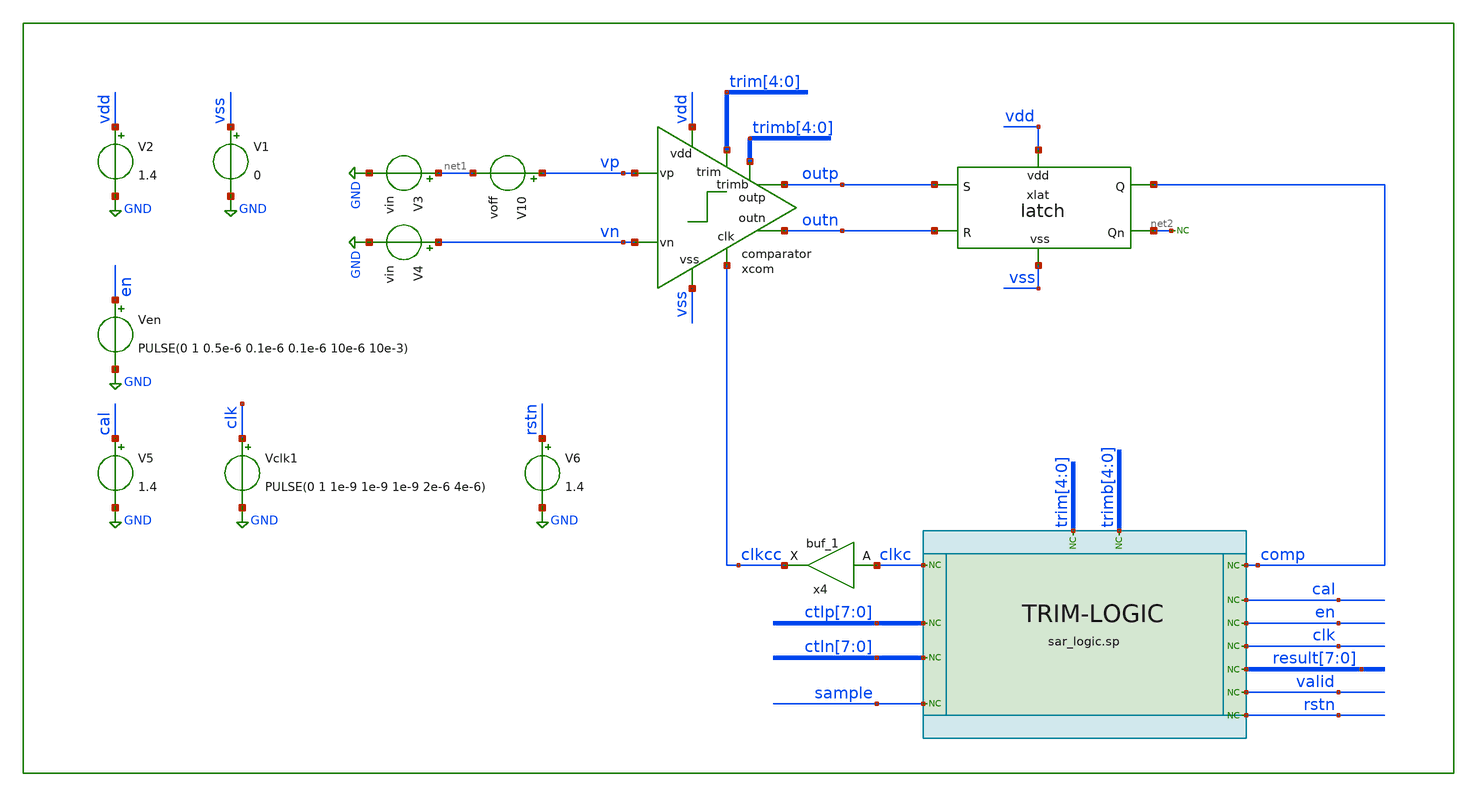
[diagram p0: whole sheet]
** sch_path: xschem/tb/comparator/tran_comparator_trim.sch
**.subckt tran_comparator_trim
xcom vss vdd clkcc outp vp outn vn trim[4] trim[3] trim[2] trim[1] trim[0] trimb[4] trimb[3]
+ trimb[2] trimb[1] trimb[0] comparator
V1 vss GND 0
V2 vdd GND 1.4
V3 net1 GND vin
V4 vn GND vin
V10 vp net1 voff
* noconn comp
x4 clkc vss vss vdd vdd clkcc sky130_fd_sc_hd__buf_1
* noconn sample
* noconn ctln[7:0]
* noconn ctlp[7:0]
* noconn trim[4:0]
* noconn trimb[4:0]
* noconn result[7:0]
* noconn valid
* noconn clkc
* noconn clk
* noconn en
* noconn cal
xlat vdd comp net2 vss outn outp latch
* noconn #net2
Vclk1 clk GND PULSE(0 1 1e-9 1e-9 1e-9 2e-6 4e-6)
V5 cal GND 1.4
Ven en GND PULSE(0 1 0.5e-6 0.1e-6 0.1e-6 10e-6 10e-3)
* noconn rstn
V6 rstn GND 1.4
**** begin user architecture code
 .include $::DESIGN_PATH/sar_10b/control/cmos_cells_digital.sp
.include $::DESIGN_PATH/sar_10b/control/sarlogic.sp
*.include $::DESIGN_PATH/sar_10b/comparator/trim_pex.sp


.param MC_SWITCH=0
.param vin=0.6
.param voff=-0.03

.options method trap

.control
tran 100e-9 200e-6
meas tran tdiff_a TRIG v(xcom.ip) val=1 fall=2 targ v(xcom.in) val=1 fall=2
meas tran tdiff_b TRIG v(xcom.ip) val=1 fall=-2 targ v(xcom.in) val=1 fall=-2

let tuntr=abs(tdiff_a)
let tres=abs(tdiff_b)
print tuntr
print tres

*plt xcom.in xcom.ip outp

*eprvcd dclk den dsamp dcomp dsamp dvalid dtrim4 dtrim3 dtrim2 dtrim1 dtrim0 dtrimb4 dtrimb3 dtrimb2
*+ dtrimb1 dtrimb0 > sarlogic.vcd
* display > "$design_path/sim/sar_nets.txt"
* edisplay > "$design_path/sim/sar_enets.txt"

*shell gtkwave "$design_path/sim/sarlogic.vcd" --script
*+ "$design_path/tools/scripts/gtkwave/nggtk.tcl" &



.endc


Xuut dclk drstn den dcomp dcal dvalid dres0 dres1 dres2 dres3 dres4 dres5 dres6 dres7 dsamp dctlp0
+ dctlp1 dctlp2 dctlp3 dctlp4 dctlp5 dctlp6 dctlp7 dctln0 dctln1 dctln2 dctln3 dctln4 dctln5 dctln6 dctln7
+ dtrim0 dtrim1 dtrim2 dtrim3 dtrim4 dtrimb0 dtrimb1 dtrimb2 dtrimb3 dtrimb4 dclkc sar_logic

.model adc_buff adc_bridge(in_low = 0.2 in_high=0.8)
.model dac_buff dac_bridge(out_high = 1.2)

Aad [clk rstn en comp cal] [dclk drstn den dcomp dcal] adc_buff
Ada [dctlp0 dctlp1 dctlp2 dctlp3 dctlp4 dctlp5 dctlp6 dctlp7 dctln0 dctln1 dctln2 dctln3 dctln4
+ dctln5 dctln6 dctln7 dres0 dres1 dres2 dres3 dres4 dres5 dres6 dres7 dsamp dclkc] [ctlp_0_ ctlp_1_ ctlp_2_
+ ctlp_3_ ctlp_4_ ctlp_5_ ctlp_6_ ctlp_7_ ctln_0_ ctln_1_ ctln_2_ ctln_3_ ctln_4_ ctln_5_ ctln_6_ ctln_7_
+ res0 res1 res2 res3 res4 res5 res6 res7 sample clkc] dac_buff
Ada2 [dtrim4 dtrim3 dtrim2 dtrim1 dtrim0 dtrimb4 dtrimb3 dtrimb2 dtrimb1 dtrimb0] [trim_4_ trim_3_
+ trim_2_ trim_1_ trim_0_ trimb_4_ trimb_3_ trimb_2_ trimb_1_ trimb_0_ ] dac_buff



* FET CORNERS
.include $::SKYWATER_MODELS/corners/tt.spice
*.include $::SKYWATER_MODELS/corners/ff.spice
*.include $::SKYWATER_MODELS/corners/ss.spice
*.include $::SKYWATER_MODELS/corners/sf.spice
*.include $::SKYWATER_MODELS/corners/fs.spice

* TT + R + C
*.include $::SKYWATER_MODELS/corners/tt_rmax_cmax.spice
*.include $::SKYWATER_MODELS/corners/tt_rmin_cmin.spice
*.include $::SKYWATER_MODELS/corners/tt_rmax_cmin.spice
*.include $::SKYWATER_MODELS/corners/tt_rmin_cmax.spice

* FF + R + C
*.include $::SKYWATER_MODELS/corners/ff_rmax_cmax.spice
*.include $::SKYWATER_MODELS/corners/ff_rmin_cmin.spice
*.include $::SKYWATER_MODELS/corners/ff_rmax_cmin.spice
*.include $::SKYWATER_MODELS/corners/ff_rmin_cmax.spice


* SS + R + C
*.include $::SKYWATER_MODELS/corners/ss_rmax_cmax.spice
*.include $::SKYWATER_MODELS/corners/ss_rmin_cmin.spice
*.include $::SKYWATER_MODELS/corners/ss_rmax_cmin.spice
*.include $::SKYWATER_MODELS/corners/ss_rmin_cmax.spice

* SF + R + C
*.include $::SKYWATER_MODELS/corners/sf_rmax_cmax.spice
*.include $::SKYWATER_MODELS/corners/sf_rmin_cmin.spice
*.include $::SKYWATER_MODELS/corners/sf_rmax_cmin.spice
*.include $::SKYWATER_MODELS/corners/sf_rmin_cmax.spice

* FS + R + C
*.include $::SKYWATER_MODELS/corners/fs_rmax_cmax.spice
*.include $::SKYWATER_MODELS/corners/fs_rmin_cmin.spice
*.include $::SKYWATER_MODELS/corners/fs_rmax_cmin.spice
*.include $::SKYWATER_MODELS/corners/fs_rmin_cmax.spice

[sky130_models]
**** end user architecture code
**.ends

* expanding   symbol:  sar_10b/comparator/comparator.sym # of pins=9
** sym_path: xschem/sar_10b/comparator/comparator.sym
** sch_path: xschem/sar_10b/comparator/comparator.sch
.subckt comparator vss vdd clk outp vp outn vn trim[4] trim[3] trim[2] trim[1] trim[0] trimb[4]
+ trimb[3] trimb[2] trimb[1] trimb[0]
*.ipin vn
*.ipin vp
*.ipin clk
*.iopin vdd
*.iopin vss
*.opin outp
*.opin outn
*.ipin trim[4],trim[3],trim[2],trim[1],trim[0]
*.ipin trimb[4],trimb[3],trimb[2],trimb[1],trimb[0]
XMdiff diff clk vss vss sky130_fd_pr__nfet_01v8 L=0.3 W=1 nf=1 ad='int((nf+1)/2) * W/nf * 0.29' as='int((nf+2)/2) * W/nf * 0.29'
+ pd='2*int((nf+1)/2) * (W/nf + 0.29)' ps='2*int((nf+2)/2) * (W/nf + 0.29)' nrd='0.29 / W' nrs='0.29 / W'
+ sa=0 sb=0 sd=0 mult=2 m=2
XMinn in vn diff vss sky130_fd_pr__nfet_01v8 L=0.3 W=1 nf=1 ad='int((nf+1)/2) * W/nf * 0.29' as='int((nf+2)/2) * W/nf * 0.29'
+ pd='2*int((nf+1)/2) * (W/nf + 0.29)' ps='2*int((nf+2)/2) * (W/nf + 0.29)' nrd='0.29 / W' nrs='0.29 / W'
+ sa=0 sb=0 sd=0 mult=1 m=1
XMinp ip vp diff vss sky130_fd_pr__nfet_01v8 L=0.3 W=1 nf=1 ad='int((nf+1)/2) * W/nf * 0.29' as='int((nf+2)/2) * W/nf * 0.29'
+ pd='2*int((nf+1)/2) * (W/nf + 0.29)' ps='2*int((nf+2)/2) * (W/nf + 0.29)' nrd='0.29 / W' nrs='0.29 / W'
+ sa=0 sb=0 sd=0 mult=1 m=1
XMl4 outp outn vdd vdd sky130_fd_pr__pfet_01v8 L=0.3 W=1 nf=1 ad='int((nf+1)/2) * W/nf * 0.29' as='int((nf+2)/2) * W/nf * 0.29'
+ pd='2*int((nf+1)/2) * (W/nf + 0.29)' ps='2*int((nf+2)/2) * (W/nf + 0.29)' nrd='0.29 / W' nrs='0.29 / W'
+ sa=0 sb=0 sd=0 mult=1 m=1
XMl3 outn outp vdd vdd sky130_fd_pr__pfet_01v8 L=0.3 W=1 nf=1 ad='int((nf+1)/2) * W/nf * 0.29' as='int((nf+2)/2) * W/nf * 0.29'
+ pd='2*int((nf+1)/2) * (W/nf + 0.29)' ps='2*int((nf+2)/2) * (W/nf + 0.29)' nrd='0.29 / W' nrs='0.29 / W'
+ sa=0 sb=0 sd=0 mult=1 m=1
XM3 outp clk vdd vdd sky130_fd_pr__pfet_01v8 L=0.3 W=1 nf=1 ad='int((nf+1)/2) * W/nf * 0.29' as='int((nf+2)/2) * W/nf * 0.29'
+ pd='2*int((nf+1)/2) * (W/nf + 0.29)' ps='2*int((nf+2)/2) * (W/nf + 0.29)' nrd='0.29 / W' nrs='0.29 / W'
+ sa=0 sb=0 sd=0 mult=1 m=1
XM2 outn clk vdd vdd sky130_fd_pr__pfet_01v8 L=0.3 W=1 nf=1 ad='int((nf+1)/2) * W/nf * 0.29' as='int((nf+2)/2) * W/nf * 0.29'
+ pd='2*int((nf+1)/2) * (W/nf + 0.29)' ps='2*int((nf+2)/2) * (W/nf + 0.29)' nrd='0.29 / W' nrs='0.29 / W'
+ sa=0 sb=0 sd=0 mult=1 m=1
XMl1 outn outp in vss sky130_fd_pr__nfet_01v8 L=0.3 W=1 nf=1 ad='int((nf+1)/2) * W/nf * 0.29' as='int((nf+2)/2) * W/nf * 0.29'
+ pd='2*int((nf+1)/2) * (W/nf + 0.29)' ps='2*int((nf+2)/2) * (W/nf + 0.29)' nrd='0.29 / W' nrs='0.29 / W'
+ sa=0 sb=0 sd=0 mult=1 m=1
XMl2 outp outn ip vss sky130_fd_pr__nfet_01v8 L=0.3 W=1 nf=1 ad='int((nf+1)/2) * W/nf * 0.29' as='int((nf+2)/2) * W/nf * 0.29'
+ pd='2*int((nf+1)/2) * (W/nf + 0.29)' ps='2*int((nf+2)/2) * (W/nf + 0.29)' nrd='0.29 / W' nrs='0.29 / W'
+ sa=0 sb=0 sd=0 mult=1 m=1
XM4 ip clk vdd vdd sky130_fd_pr__pfet_01v8 L=0.3 W=1 nf=1 ad='int((nf+1)/2) * W/nf * 0.29' as='int((nf+2)/2) * W/nf * 0.29'
+ pd='2*int((nf+1)/2) * (W/nf + 0.29)' ps='2*int((nf+2)/2) * (W/nf + 0.29)' nrd='0.29 / W' nrs='0.29 / W'
+ sa=0 sb=0 sd=0 mult=1 m=1
XM1 in clk vdd vdd sky130_fd_pr__pfet_01v8 L=0.3 W=1 nf=1 ad='int((nf+1)/2) * W/nf * 0.29' as='int((nf+2)/2) * W/nf * 0.29'
+ pd='2*int((nf+1)/2) * (W/nf + 0.29)' ps='2*int((nf+2)/2) * (W/nf + 0.29)' nrd='0.29 / W' nrs='0.29 / W'
+ sa=0 sb=0 sd=0 mult=1 m=1
x2 in trim[4] trim[3] trim[2] trim[1] trim[0] vss trim
x3 ip trimb[4] trimb[3] trimb[2] trimb[1] trimb[0] vss trim
.ends


* expanding   symbol:  sar_10b/latch/latch.sym # of pins=6
** sym_path: xschem/sar_10b/latch/latch.sym
** sch_path: xschem/sar_10b/latch/latch.sch
.subckt latch vdd Q Qn vss R S
*.ipin S
*.ipin R
*.iopin vss
*.iopin vdd
*.opin Q
*.opin Qn
x1 vdd Qn Q vss inv_lvt
x2 vdd Q Qn vss inv_lvt
x3 vdd R net2 vss inv_lvt
x4 vdd S net1 vss inv_lvt
XM3 Qn net1 vss vss sky130_fd_pr__nfet_01v8_lvt L=0.4 W=1 nf=1 ad='int((nf+1)/2) * W/nf * 0.29' as='int((nf+2)/2) * W/nf * 0.29'
+ pd='2*int((nf+1)/2) * (W/nf + 0.29)' ps='2*int((nf+2)/2) * (W/nf + 0.29)' nrd='0.29 / W' nrs='0.29 / W'
+ sa=0 sb=0 sd=0 mult=1 m=1
XM1 Q net2 vss vss sky130_fd_pr__nfet_01v8_lvt L=0.4 W=1 nf=1 ad='int((nf+1)/2) * W/nf * 0.29' as='int((nf+2)/2) * W/nf * 0.29'
+ pd='2*int((nf+1)/2) * (W/nf + 0.29)' ps='2*int((nf+2)/2) * (W/nf + 0.29)' nrd='0.29 / W' nrs='0.29 / W'
+ sa=0 sb=0 sd=0 mult=1 m=1
.ends


* expanding   symbol:  sar_10b/comparator/trim.sym # of pins=3
** sym_path: xschem/sar_10b/comparator/trim.sym
** sch_path: xschem/sar_10b/comparator/trim.sch
.subckt trim drain d[4] d[3] d[2] d[1] d[0] vss
*.iopin vss
*.ipin d[4],d[3],d[2],d[1],d[0]
*.opin drain
XM4[7] n4 d[4] vss vss sky130_fd_pr__nfet_01v8_lvt L=0.3 W=1 nf=1 ad='int((nf+1)/2) * W/nf * 0.29' as='int((nf+2)/2) * W/nf * 0.29'
+ pd='2*int((nf+1)/2) * (W/nf + 0.29)' ps='2*int((nf+2)/2) * (W/nf + 0.29)' nrd='0.29 / W' nrs='0.29 / W'
+ sa=0 sb=0 sd=0 mult=1 m=1
XM4[6] n4 d[4] vss vss sky130_fd_pr__nfet_01v8_lvt L=0.3 W=1 nf=1 ad='int((nf+1)/2) * W/nf * 0.29' as='int((nf+2)/2) * W/nf * 0.29'
+ pd='2*int((nf+1)/2) * (W/nf + 0.29)' ps='2*int((nf+2)/2) * (W/nf + 0.29)' nrd='0.29 / W' nrs='0.29 / W'
+ sa=0 sb=0 sd=0 mult=1 m=1
XM4[5] n4 d[4] vss vss sky130_fd_pr__nfet_01v8_lvt L=0.3 W=1 nf=1 ad='int((nf+1)/2) * W/nf * 0.29' as='int((nf+2)/2) * W/nf * 0.29'
+ pd='2*int((nf+1)/2) * (W/nf + 0.29)' ps='2*int((nf+2)/2) * (W/nf + 0.29)' nrd='0.29 / W' nrs='0.29 / W'
+ sa=0 sb=0 sd=0 mult=1 m=1
XM4[4] n4 d[4] vss vss sky130_fd_pr__nfet_01v8_lvt L=0.3 W=1 nf=1 ad='int((nf+1)/2) * W/nf * 0.29' as='int((nf+2)/2) * W/nf * 0.29'
+ pd='2*int((nf+1)/2) * (W/nf + 0.29)' ps='2*int((nf+2)/2) * (W/nf + 0.29)' nrd='0.29 / W' nrs='0.29 / W'
+ sa=0 sb=0 sd=0 mult=1 m=1
XM4[3] n4 d[4] vss vss sky130_fd_pr__nfet_01v8_lvt L=0.3 W=1 nf=1 ad='int((nf+1)/2) * W/nf * 0.29' as='int((nf+2)/2) * W/nf * 0.29'
+ pd='2*int((nf+1)/2) * (W/nf + 0.29)' ps='2*int((nf+2)/2) * (W/nf + 0.29)' nrd='0.29 / W' nrs='0.29 / W'
+ sa=0 sb=0 sd=0 mult=1 m=1
XM4[2] n4 d[4] vss vss sky130_fd_pr__nfet_01v8_lvt L=0.3 W=1 nf=1 ad='int((nf+1)/2) * W/nf * 0.29' as='int((nf+2)/2) * W/nf * 0.29'
+ pd='2*int((nf+1)/2) * (W/nf + 0.29)' ps='2*int((nf+2)/2) * (W/nf + 0.29)' nrd='0.29 / W' nrs='0.29 / W'
+ sa=0 sb=0 sd=0 mult=1 m=1
XM4[1] n4 d[4] vss vss sky130_fd_pr__nfet_01v8_lvt L=0.3 W=1 nf=1 ad='int((nf+1)/2) * W/nf * 0.29' as='int((nf+2)/2) * W/nf * 0.29'
+ pd='2*int((nf+1)/2) * (W/nf + 0.29)' ps='2*int((nf+2)/2) * (W/nf + 0.29)' nrd='0.29 / W' nrs='0.29 / W'
+ sa=0 sb=0 sd=0 mult=1 m=1
XM4[0] n4 d[4] vss vss sky130_fd_pr__nfet_01v8_lvt L=0.3 W=1 nf=1 ad='int((nf+1)/2) * W/nf * 0.29' as='int((nf+2)/2) * W/nf * 0.29'
+ pd='2*int((nf+1)/2) * (W/nf + 0.29)' ps='2*int((nf+2)/2) * (W/nf + 0.29)' nrd='0.29 / W' nrs='0.29 / W'
+ sa=0 sb=0 sd=0 mult=1 m=1
XM3[3] n3 d[3] vss vss sky130_fd_pr__nfet_01v8_lvt L=0.3 W=1 nf=1 ad='int((nf+1)/2) * W/nf * 0.29' as='int((nf+2)/2) * W/nf * 0.29'
+ pd='2*int((nf+1)/2) * (W/nf + 0.29)' ps='2*int((nf+2)/2) * (W/nf + 0.29)' nrd='0.29 / W' nrs='0.29 / W'
+ sa=0 sb=0 sd=0 mult=1 m=1
XM3[2] n3 d[3] vss vss sky130_fd_pr__nfet_01v8_lvt L=0.3 W=1 nf=1 ad='int((nf+1)/2) * W/nf * 0.29' as='int((nf+2)/2) * W/nf * 0.29'
+ pd='2*int((nf+1)/2) * (W/nf + 0.29)' ps='2*int((nf+2)/2) * (W/nf + 0.29)' nrd='0.29 / W' nrs='0.29 / W'
+ sa=0 sb=0 sd=0 mult=1 m=1
XM3[1] n3 d[3] vss vss sky130_fd_pr__nfet_01v8_lvt L=0.3 W=1 nf=1 ad='int((nf+1)/2) * W/nf * 0.29' as='int((nf+2)/2) * W/nf * 0.29'
+ pd='2*int((nf+1)/2) * (W/nf + 0.29)' ps='2*int((nf+2)/2) * (W/nf + 0.29)' nrd='0.29 / W' nrs='0.29 / W'
+ sa=0 sb=0 sd=0 mult=1 m=1
XM3[0] n3 d[3] vss vss sky130_fd_pr__nfet_01v8_lvt L=0.3 W=1 nf=1 ad='int((nf+1)/2) * W/nf * 0.29' as='int((nf+2)/2) * W/nf * 0.29'
+ pd='2*int((nf+1)/2) * (W/nf + 0.29)' ps='2*int((nf+2)/2) * (W/nf + 0.29)' nrd='0.29 / W' nrs='0.29 / W'
+ sa=0 sb=0 sd=0 mult=1 m=1
XM2[1] n2 d[2] vss vss sky130_fd_pr__nfet_01v8_lvt L=0.3 W=1 nf=1 ad='int((nf+1)/2) * W/nf * 0.29' as='int((nf+2)/2) * W/nf * 0.29'
+ pd='2*int((nf+1)/2) * (W/nf + 0.29)' ps='2*int((nf+2)/2) * (W/nf + 0.29)' nrd='0.29 / W' nrs='0.29 / W'
+ sa=0 sb=0 sd=0 mult=1 m=1
XM2[0] n2 d[2] vss vss sky130_fd_pr__nfet_01v8_lvt L=0.3 W=1 nf=1 ad='int((nf+1)/2) * W/nf * 0.29' as='int((nf+2)/2) * W/nf * 0.29'
+ pd='2*int((nf+1)/2) * (W/nf + 0.29)' ps='2*int((nf+2)/2) * (W/nf + 0.29)' nrd='0.29 / W' nrs='0.29 / W'
+ sa=0 sb=0 sd=0 mult=1 m=1
XM1 n1 d[1] vss vss sky130_fd_pr__nfet_01v8_lvt L=0.3 W=1 nf=1 ad='int((nf+1)/2) * W/nf * 0.29' as='int((nf+2)/2) * W/nf * 0.29'
+ pd='2*int((nf+1)/2) * (W/nf + 0.29)' ps='2*int((nf+2)/2) * (W/nf + 0.29)' nrd='0.29 / W' nrs='0.29 / W'
+ sa=0 sb=0 sd=0 mult=1 m=1
XM0 n0 d[0] vss vss sky130_fd_pr__nfet_01v8_lvt L=0.3 W=1 nf=1 ad='int((nf+1)/2) * W/nf * 0.29' as='int((nf+2)/2) * W/nf * 0.29'
+ pd='2*int((nf+1)/2) * (W/nf + 0.29)' ps='2*int((nf+2)/2) * (W/nf + 0.29)' nrd='0.29 / W' nrs='0.29 / W'
+ sa=0 sb=0 sd=0 mult=1 m=1
x4[7] drain n4 trimcap
x4[6] drain n4 trimcap
x4[5] drain n4 trimcap
x4[4] drain n4 trimcap
x4[3] drain n4 trimcap
x4[2] drain n4 trimcap
x4[1] drain n4 trimcap
x4[0] drain n4 trimcap
x3[3] drain n3 trimcap
x3[2] drain n3 trimcap
x3[1] drain n3 trimcap
x3[0] drain n3 trimcap
x2[1] drain n2 trimcap
x2[0] drain n2 trimcap
x1 drain n1 trimcap
x0 drain n0 trimcap
.ends


* expanding   symbol:  logic/inv_lvt.sym # of pins=4
** sym_path: xschem/logic/inv_lvt.sym
** sch_path: xschem/logic/inv_lvt.sch
.subckt inv_lvt vdd in out vss
*.iopin vdd
*.iopin vss
*.ipin in
*.opin out
XM1 out in vss vss sky130_fd_pr__nfet_01v8_lvt L=0.4 W=1 nf=1 ad='int((nf+1)/2) * W/nf * 0.29' as='int((nf+2)/2) * W/nf * 0.29'
+ pd='2*int((nf+1)/2) * (W/nf + 0.29)' ps='2*int((nf+2)/2) * (W/nf + 0.29)' nrd='0.29 / W' nrs='0.29 / W'
+ sa=0 sb=0 sd=0 mult=1 m=1
XM2 out in vdd vdd sky130_fd_pr__pfet_01v8_lvt L=0.4 W=1 nf=1 ad='int((nf+1)/2) * W/nf * 0.29' as='int((nf+2)/2) * W/nf * 0.29'
+ pd='2*int((nf+1)/2) * (W/nf + 0.29)' ps='2*int((nf+2)/2) * (W/nf + 0.29)' nrd='0.29 / W' nrs='0.29 / W'
+ sa=0 sb=0 sd=0 mult=1 m=1
.ends


* expanding   symbol:  sar_10b/comparator/trimcap.sym # of pins=2
** sym_path: xschem/sar_10b/comparator/trimcap.sym
** sch_path: xschem/sar_10b/comparator/trimcap.sch
.subckt trimcap cp cn
*.iopin cp
*.iopin cn
c0 net1 cn 2f m=1
c1 cp net1 1f m=1
.ends

.GLOBAL GND
.end
